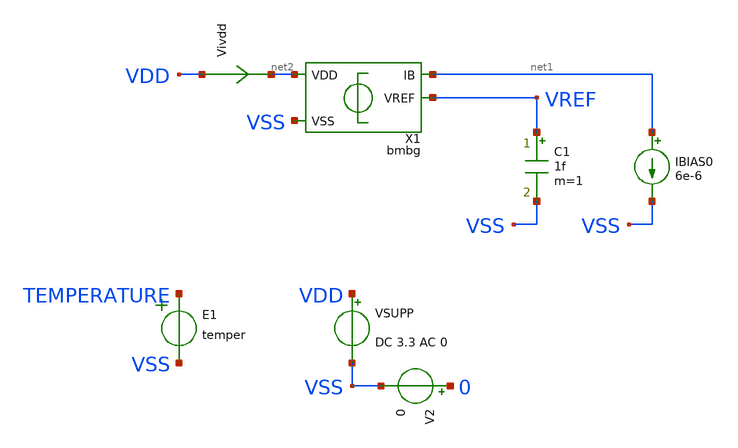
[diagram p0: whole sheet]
** sch_path: ip/bmbg/xschem/bmbg_tb.sch
**.subckt bmbg_tb
VSUPP VDD VSS DC 3.3 AC 0
V2 0 VSS 0
E1 TEMPERATURE VSS VOL=' temper '
IBIAS0 net1 VSS 6e-6
C1 VREF VSS 1f m=1
X1 net2 VSS net1 VREF bmbg
Vivdd VDD net2 0
.save i(vivdd)
**** begin user architecture code

.csparam TB_ID=${::TB_ID}
.csparam MC_RUNS=${::MC_RUNS}
.csparam EXIT_NGSPICE=${::EXIT_NGSPICE}
.lib ${::IHP_MODELS}/sg13g2.lib ${::CORNER}


* this experimental option enables mos model bin
* selection based on W/NF instead of W
.option wnflag=0

.control
option savecurrents
save all

* dummy block for goto
if (1)
if TB_ID = 0
	goto TRAN_CURVE_TEMP
end
if TB_ID = 1
	goto TRAN_CURVE_TEMP
end
if TB_ID = 2
	goto VREF_NOISE
end
if TB_ID = 3
	goto AC_PSRR
end
if TB_ID = 4
	goto TRAN_CURVE_VDD
end
if TB_ID = 5
	goto TRAN_STARTUP
end

****************************************
label TRAN_CURVE_TEMP
save all
****************************************
if MC_RUNS = 0
	let veclen=3
	let vref_pp = vector(veclen)
	let vref_t20 = vector(veclen)
	let vref_tc20 = vector(veclen)
	let vref_mean = vector(veclen)
	let vsup = vector(veclen)
	let isup = vector(veclen)
	let run = 0

	foreach v_sweep 1.8 2.5 3.3
	*foreach v_sweep 1.8

		.include tran_curve_temp_ops.inc

		let run = run + 1
	end

	set nobreak
	set width=300
	print isup, vsup, vref_pp, vref_mean, vref_t20, vref_tc20 > dc.csv

else
	let vref_pp = vector(MC_RUNS)
	let vref_t20 = vector(MC_RUNS)
	let vref_tc20 = vector(MC_RUNS)
	let vref_mean = vector(MC_RUNS)
	let vsup = vector(MC_RUNS)
	let isup = vector(MC_RUNS)
	let run = 0
	set v_sweep = 3.3

	dowhile run < MC_RUNS
		echo MC-RUN: $&run

		.include tran_curve_temp_ops.inc

 		reset
		let run = run + 1
	end

	set nobreak
	set width=300
	print isup, vsup, vref_pp, vref_mean, vref_t20, vref_tc20 > dc.csv
end
goto done

****************************************
label TRAN_CURVE_VDD
save all
****************************************
if MC_RUNS = 0
	let veclen=3
	let vref_pp = vector(veclen)
	let vref_3v3 = vector(veclen)
	let vref_tc3v3 = vector(veclen)
	let vref_mean = vector(veclen)
	let te = vector(veclen)
	let isup = vector(veclen)
	let run = 0

	foreach t_sweep -40 20 125
	*foreach t_sweep 20

		.include tran_curve_vdd_ops.inc

		let run = run + 1
	end

	set nobreak
	set width=300
	print isup, te, vref_pp, vref_mean, vref_3v3, vref_tc3v3 > dc.csv

else
	let vref_pp = vector(MC_RUNS)
	let vref_3v3 = vector(MC_RUNS)
	let vref_tc3v3 = vector(MC_RUNS)
	let vref_mean = vector(MC_RUNS)
	let te = vector(MC_RUNS)
	let isup = vector(MC_RUNS)
	let run = 0
	set t_sweep = 20

	dowhile run < MC_RUNS
		echo MC-RUN: $&run

		.include tran_curve_vdd_ops.inc

 		reset
		let run = run + 1
	end

	set nobreak
	set width=300
	print isup, te, vref_pp, vref_mean, vref_3v3, vref_tc3v3 > dc.csv
end
goto done

****************************************
label VREF_NOISE
****************************************
noise v(vref) VSUPP dec 10 1 100e3 1
setplot noise2
print onoise_total
setplot noise1
plot onoise_spectrum
write noise1_isource.raw all

* https://sourceforge.net/p/ngspice/discussion/120973/thread/2aa3e30f/ -- Holger Vogt
* script to read a specific y-value if x given
**********************************************
let f0 = vector(1)
let f1 = vector(1)
let n_f0 = vector(1)
let n_f1 = vector(1)
compose freq_list values 10 10e3
foreach freq_idx 0 1
	let freq = freq_list[$freq_idx]
	* find index where freqency is just above interesting value
	setplot noise1
	let nn = 0
	while frequency[nn] < freq
		let nn = nn + 1
	end
	* define vectors of frequncies and values just above and below
	* selected frequeny
	let fnn = frequency[nn]
	let nn1 = nn - 1
	let fnn1 = frequency[nn1]
	let snn = onoise_spectrum[nn]
	let snn1 = onoise_spectrum[nn1]
	*print vector values
	echo nn = $&nn  fnn = $&fnn  snn = $&snn
	echo nn1 = $&nn1  fnn1 = $&fnn1  snn1 = $&snn1
	*linear interpolation for exact frequency
	let newsnn = snn1 + (snn - snn1)/(fnn - fnn1)*(freq - fnn1)
	echo newfnn = $&freq  newsnn = $&newsnn
	if $freq_idx = 0
		let f0 = freq
		let n_f0 = newsnn
	end
	if $freq_idx = 1
		let f1 = freq
		let n_f1 = newsnn
	end
end
set nobreak
set width=300
set noprintscale
print col f0, n_f0, f1, n_f1 > ac_inoise.csv

goto done

****************************************
label AC_PSRR
save all
****************************************
if MC_RUNS = 0
	let psrr_p_10Hz = vector(MC_RUNS+1)
	let psrr_p_10MHz = vector(MC_RUNS+1)
	let run=0

	.include ac_psrr_ops.inc

	set nobreak
	set width=300
	print col psrr_p_10Hz, psrr_p_10MHz > ac_psrr.csv
else
	let psrr_p_10Hz = vector(MC_RUNS)
	let psrr_p_10MHz = vector(MC_RUNS)
	let run=0
	dowhile run < MC_RUNS
		echo MC-RUN: $&run

		.include ac_psrr_ops.inc

 		reset
		let run = run + 1
	end
	set nobreak
	set width=300
	print psrr_p_10Hz, psrr_p_10MHz > ac_psrr.csv
end
goto done

****************************************
label TRAN_STARTUP
****************************************
if MC_RUNS = 0
	let veclen=4
	let startup_t = vector(veclen)
	let run=0
	foreach v_sweep 1.8 2.5 3.3
	*foreach v_sweep 1.8
		save VREF
		alter @VSUPP[pwl] = [ 0 0 100u $v_sweep]
		*alter @IBIAS0[pwl] = [ 0 0 100us 0 150us 10e-6 ]
  		tran 100n 200u
  		*plot vivdd#branch
		*plot v.x1.vmeassu1#branch
		*plot v.x1.vmeassu2#branch
		*plot v.x1.vmeasr#branch
		*plot v.x1.vmeasl#branch
		*plot v.x1.vmeasout#branch
		*plot VDD
		plot VREF
		meas tran m_vref_up when VREF=0.5 rise=1
		let startup_t[run] = m_vref_up
		write tran.raw all
		let run = run + 1
		set appendwrite
		reset
	end
	print startup_t > tran.csv
else
	let startup_t = vector(MC_RUNS)
	let run=0
	dowhile run < MC_RUNS
		echo MC-RUN: $&run
		alter @VSUPP[pwl] = [ 0 0 100u 3.3]
		save VREF
		tran 100n 200u
		meas tran m_vref_up when VREF=0.5 rise=1
		let startup_t[run] = m_vref_up
 		reset
		let run = run + 1
	end
	print startup_t > tran.csv
end
goto done

****************************************
label done
****************************************
if EXIT_NGSPICE > 0.0
	exit
end
end
.endc


**** end user architecture code
**.ends

* expanding   symbol:  bmbg.sym # of pins=4
** sym_path: ip/bmbg/xschem/bmbg.sym
** sch_path: ip/bmbg/xschem/bmbg.sch
.subckt bmbg VDD VSS IB VREF
*.iopin VSS
*.iopin VDD
*.opin VREF
*.opin IB
X1 VDD VSS vt IB vl vr bmbgota
XMSIT3 vsu vt VDD VDD sg13_hv_pmos w=5u l=0.5u ng=1 m=3 mm_ok=1
XMSIT4 VSS vsu vt VDD sg13_hv_pmos w=10u l=0.5u ng=1 m=2 mm_ok=1
XMSIT net3 vt VDD VDD sg13_hv_pmos w=10u l=2u ng=1 m=1 mm_ok=1
XMSIT1 net5 vt VDD VDD sg13_hv_pmos w=10u l=2u ng=1 m=1 mm_ok=1
XMSIT2 VREF vt VDD VDD sg13_hv_pmos w=10u l=2u ng=1 m=1 mm_ok=1
XQ1 VSS VSS vl pnpMPA a=4p p=8u m=1
XQ2 VSS VSS net1 pnpMPA a=4p p=8u m=1
XQ3 VSS VSS net1 pnpMPA a=4p p=8u m=1
XQ4 VSS VSS net1 pnpMPA a=4p p=8u m=1
XQ5 VSS VSS net1 pnpMPA a=4p p=8u m=1
XQ6 VSS VSS net1 pnpMPA a=4p p=8u m=1
XQ7 VSS VSS net1 pnpMPA a=4p p=8u m=1
XQ8 VSS VSS net1 pnpMPA a=4p p=8u m=1
XQ9 VSS VSS net1 pnpMPA a=4p p=8u m=1
XQ10 VSS VSS net2 pnpMPA a=4p p=8u m=1
Vmeasl net3 net4 0
.save i(vmeasl)
Vmeasr net5 net6 0
.save i(vmeasr)
XRSU vsu VSS VSS rhigh w=0.5e-6 l=50e-6 m=1 b=0 mm_ok=1
XR2 net4 vl VSS rppd w=1e-6 l=80e-6 m=1 b=0 mm_ok=1
XR1 net6 vr VSS rppd w=1e-6 l=80e-6 m=1 b=0 mm_ok=1
XR4 vr net1 VSS rppd w=1e-6 l=10.7e-6 m=1 b=0 mm_ok=1
XR3 VREF net2 VSS rppd w=1e-6 l=80e-6 m=1 b=0 mm_ok=1
.ends


* expanding   symbol:  bmbgota.sym # of pins=6
** sym_path: ip/bmbg/xschem/bmbgota.sym
** sch_path: ip/bmbg/xschem/bmbgota.sch
.subckt bmbgota VDD VSS VOUT IB INN INP
*.iopin INP
*.iopin INN
*.iopin VOUT
*.opin IB
*.iopin VDD
*.iopin VSS
XMMIR1 IB IB VDD VDD sg13_hv_pmos w=5u l=2u ng=1 m=1 mm_ok=1
XMMIR2 net1 IB VDD VDD sg13_hv_pmos w=5u l=2u ng=1 m=2 mm_ok=1
XMMIR3 VOUT IB VDD VDD sg13_hv_pmos w=5u l=2u ng=1 m=3 mm_ok=1
XMDL net2 INN net1 VDD sg13_hv_pmos w=10u l=1u ng=1 m=16 mm_ok=1
XMDR net3 INP net1 VDD sg13_hv_pmos w=10u l=1u ng=1 m=16 mm_ok=1
XMMIRR net3 net2 VSS VSS sg13_hv_nmos w=5u l=2u ng=1 m=4 mm_ok=1
XMMIRL net2 net2 VSS VSS sg13_hv_nmos w=5u l=2u ng=1 m=4 mm_ok=1
XMO VOUT net3 VSS VSS sg13_hv_nmos w=5u l=2u ng=1 m=4 mm_ok=1
XC1 VOUT net4 cap_cmim w=30e-6 l=21e-6 m=1 mm_ok=1
XR1 net3 net4 VSS rhigh w=0.5e-6 l=3.5e-6 m=1 b=0 mm_ok=1
.ends

.end
